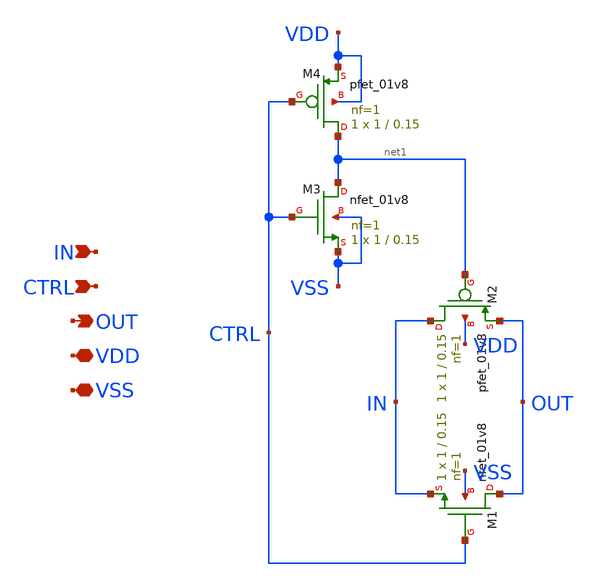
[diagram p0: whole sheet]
** sch_path: xschem/transmission_gate.sch
**.subckt transmission_gate IN CTRL OUT VDD VSS
*.ipin IN
*.ipin CTRL
*.opin OUT
*.iopin VDD
*.iopin VSS
XM1 OUT CTRL IN VSS sky130_fd_pr__nfet_01v8 L=0.15 W=1 nf=1 ad='int((nf+1)/2) * W/nf * 0.29' as='int((nf+2)/2) * W/nf * 0.29'
+ pd='2*int((nf+1)/2) * (W/nf + 0.29)' ps='2*int((nf+2)/2) * (W/nf + 0.29)' nrd='0.29 / W' nrs='0.29 / W'
+ sa=0 sb=0 sd=0 mult=1 m=1
XM2 IN net1 OUT VDD sky130_fd_pr__pfet_01v8 L=0.15 W=1 nf=1 ad='int((nf+1)/2) * W/nf * 0.29' as='int((nf+2)/2) * W/nf * 0.29'
+ pd='2*int((nf+1)/2) * (W/nf + 0.29)' ps='2*int((nf+2)/2) * (W/nf + 0.29)' nrd='0.29 / W' nrs='0.29 / W'
+ sa=0 sb=0 sd=0 mult=1 m=1
XM3 net1 CTRL VSS VSS sky130_fd_pr__nfet_01v8 L=0.15 W=1 nf=1 ad='int((nf+1)/2) * W/nf * 0.29' as='int((nf+2)/2) * W/nf * 0.29'
+ pd='2*int((nf+1)/2) * (W/nf + 0.29)' ps='2*int((nf+2)/2) * (W/nf + 0.29)' nrd='0.29 / W' nrs='0.29 / W'
+ sa=0 sb=0 sd=0 mult=1 m=1
XM4 net1 CTRL VDD VDD sky130_fd_pr__pfet_01v8 L=0.15 W=1 nf=1 ad='int((nf+1)/2) * W/nf * 0.29' as='int((nf+2)/2) * W/nf * 0.29'
+ pd='2*int((nf+1)/2) * (W/nf + 0.29)' ps='2*int((nf+2)/2) * (W/nf + 0.29)' nrd='0.29 / W' nrs='0.29 / W'
+ sa=0 sb=0 sd=0 mult=1 m=1
**.ends
.end
